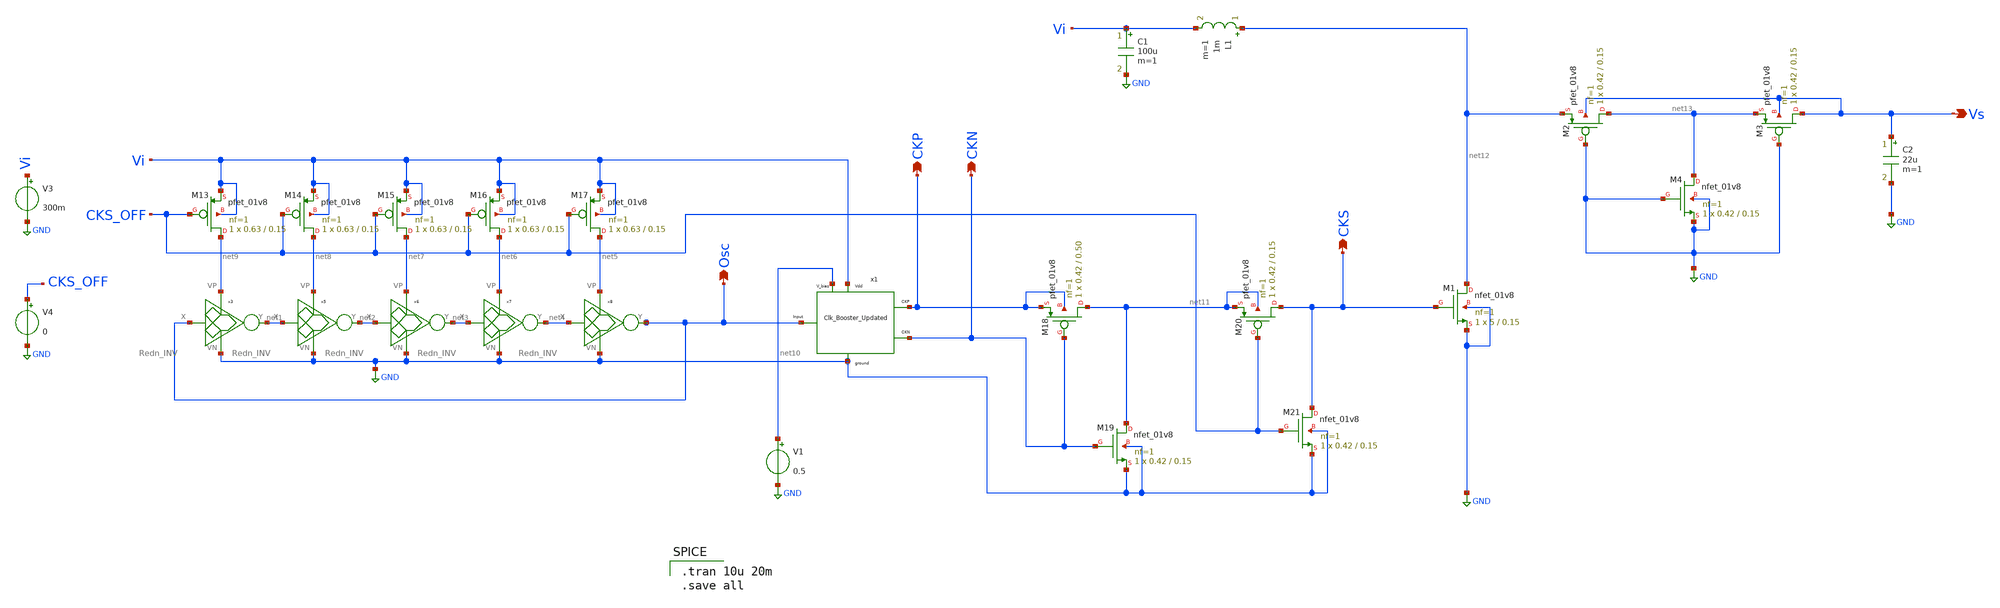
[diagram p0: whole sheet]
** sch_path: Blocks/StartupConverter/Startup_Converter1.sch
**.subckt Startup_Converter1 CKP CKN Osc CKS Vs
*.opin CKP
*.opin CKN
*.opin Osc
*.opin CKS
*.opin Vs
V3 Vi GND 300m
x3 Osc net1 net9 GND Redn_INV
x5 net1 net2 net8 GND Redn_INV
x6 net2 net3 net7 GND Redn_INV
x7 net3 net4 net6 GND Redn_INV
x8 net4 Osc net5 GND Redn_INV
XM13 net9 CKS_OFF Vi Vi sky130_fd_pr__pfet_01v8 L=0.15 W=0.63 nf=1 ad='int((nf+1)/2) * W/nf * 0.29' as='int((nf+2)/2) * W/nf * 0.29'
+ pd='2*int((nf+1)/2) * (W/nf + 0.29)' ps='2*int((nf+2)/2) * (W/nf + 0.29)' nrd='0.29 / W' nrs='0.29 / W'
+ sa=0 sb=0 sd=0 mult=1 m=1
XM14 net8 CKS_OFF Vi Vi sky130_fd_pr__pfet_01v8 L=0.15 W=0.63 nf=1 ad='int((nf+1)/2) * W/nf * 0.29' as='int((nf+2)/2) * W/nf * 0.29'
+ pd='2*int((nf+1)/2) * (W/nf + 0.29)' ps='2*int((nf+2)/2) * (W/nf + 0.29)' nrd='0.29 / W' nrs='0.29 / W'
+ sa=0 sb=0 sd=0 mult=1 m=1
XM15 net7 CKS_OFF Vi Vi sky130_fd_pr__pfet_01v8 L=0.15 W=0.63 nf=1 ad='int((nf+1)/2) * W/nf * 0.29' as='int((nf+2)/2) * W/nf * 0.29'
+ pd='2*int((nf+1)/2) * (W/nf + 0.29)' ps='2*int((nf+2)/2) * (W/nf + 0.29)' nrd='0.29 / W' nrs='0.29 / W'
+ sa=0 sb=0 sd=0 mult=1 m=1
XM16 net6 CKS_OFF Vi Vi sky130_fd_pr__pfet_01v8 L=0.15 W=0.63 nf=1 ad='int((nf+1)/2) * W/nf * 0.29' as='int((nf+2)/2) * W/nf * 0.29'
+ pd='2*int((nf+1)/2) * (W/nf + 0.29)' ps='2*int((nf+2)/2) * (W/nf + 0.29)' nrd='0.29 / W' nrs='0.29 / W'
+ sa=0 sb=0 sd=0 mult=1 m=1
XM17 net5 CKS_OFF Vi Vi sky130_fd_pr__pfet_01v8 L=0.15 W=0.63 nf=1 ad='int((nf+1)/2) * W/nf * 0.29' as='int((nf+2)/2) * W/nf * 0.29'
+ pd='2*int((nf+1)/2) * (W/nf + 0.29)' ps='2*int((nf+2)/2) * (W/nf + 0.29)' nrd='0.29 / W' nrs='0.29 / W'
+ sa=0 sb=0 sd=0 mult=1 m=1
V4 CKS_OFF GND 0
V1 net10 GND 0.5
XM18 net11 CKN CKP CKP sky130_fd_pr__pfet_01v8 L=0.50 W=0.42 nf=1 ad='int((nf+1)/2) * W/nf * 0.29' as='int((nf+2)/2) * W/nf * 0.29'
+ pd='2*int((nf+1)/2) * (W/nf + 0.29)' ps='2*int((nf+2)/2) * (W/nf + 0.29)' nrd='0.29 / W' nrs='0.29 / W'
+ sa=0 sb=0 sd=0 mult=1 m=1
XM19 net11 CKN GND GND sky130_fd_pr__nfet_01v8 L=0.15 W=0.42 nf=1 ad='int((nf+1)/2) * W/nf * 0.29' as='int((nf+2)/2) * W/nf * 0.29'
+ pd='2*int((nf+1)/2) * (W/nf + 0.29)' ps='2*int((nf+2)/2) * (W/nf + 0.29)' nrd='0.29 / W' nrs='0.29 / W'
+ sa=0 sb=0 sd=0 mult=1 m=1
XM21 CKS CKS_OFF GND GND sky130_fd_pr__nfet_01v8 L=0.15 W=0.42 nf=1 ad='int((nf+1)/2) * W/nf * 0.29'
+ as='int((nf+2)/2) * W/nf * 0.29' pd='2*int((nf+1)/2) * (W/nf + 0.29)' ps='2*int((nf+2)/2) * (W/nf + 0.29)'
+ nrd='0.29 / W' nrs='0.29 / W' sa=0 sb=0 sd=0 mult=1 m=1
XM20 CKS CKS_OFF net11 net11 sky130_fd_pr__pfet_01v8 L=0.15 W=0.42 nf=1 ad='int((nf+1)/2) * W/nf * 0.29'
+ as='int((nf+2)/2) * W/nf * 0.29' pd='2*int((nf+1)/2) * (W/nf + 0.29)' ps='2*int((nf+2)/2) * (W/nf + 0.29)'
+ nrd='0.29 / W' nrs='0.29 / W' sa=0 sb=0 sd=0 mult=1 m=1
x1 Osc Vi GND CKP CKN net10 Clk_Booster_Updated
C1 Vi GND 100u m=1
L1 net12 Vi 1m m=1
XM1 net12 CKS GND GND sky130_fd_pr__nfet_01v8 L=0.15 W=5 nf=1 ad='int((nf+1)/2) * W/nf * 0.29' as='int((nf+2)/2) * W/nf * 0.29'
+ pd='2*int((nf+1)/2) * (W/nf + 0.29)' ps='2*int((nf+2)/2) * (W/nf + 0.29)' nrd='0.29 / W' nrs='0.29 / W'
+ sa=0 sb=0 sd=0 mult=1 m=1
XM2 net13 GND net12 Vs sky130_fd_pr__pfet_01v8 L=0.15 W=0.42 nf=1 ad='int((nf+1)/2) * W/nf * 0.29' as='int((nf+2)/2) * W/nf * 0.29'
+ pd='2*int((nf+1)/2) * (W/nf + 0.29)' ps='2*int((nf+2)/2) * (W/nf + 0.29)' nrd='0.29 / W' nrs='0.29 / W'
+ sa=0 sb=0 sd=0 mult=1 m=1
XM3 Vs GND net13 Vs sky130_fd_pr__pfet_01v8 L=0.15 W=0.42 nf=1 ad='int((nf+1)/2) * W/nf * 0.29' as='int((nf+2)/2) * W/nf * 0.29'
+ pd='2*int((nf+1)/2) * (W/nf + 0.29)' ps='2*int((nf+2)/2) * (W/nf + 0.29)' nrd='0.29 / W' nrs='0.29 / W'
+ sa=0 sb=0 sd=0 mult=1 m=1
XM4 net13 GND GND GND sky130_fd_pr__nfet_01v8 L=0.15 W=0.42 nf=1 ad='int((nf+1)/2) * W/nf * 0.29' as='int((nf+2)/2) * W/nf * 0.29'
+ pd='2*int((nf+1)/2) * (W/nf + 0.29)' ps='2*int((nf+2)/2) * (W/nf + 0.29)' nrd='0.29 / W' nrs='0.29 / W'
+ sa=0 sb=0 sd=0 mult=1 m=1
C2 Vs GND 22u m=1
**** begin user architecture code

** opencircuitdesign pdks install
.lib $::SKYWATER_MODELS/sky130.lib.spice tt



.tran 10u 20m
.save all

**** end user architecture code
**.ends

* expanding   symbol:  Pico_project/Rdn_INV/Redn_INV.sym # of pins=4
** sym_path: component/Reduntant_Inverter/Redn_INV.sym
** sch_path: component/Reduntant_Inverter/Redn_INV.sch
.subckt Redn_INV X Y VP VN
*.opin Y
*.ipin X
*.iopin VP
*.iopin VN
XM15 net4 X VN VN sky130_fd_pr__nfet_01v8_lvt L=0.15 W=1 nf=1 ad='int((nf+1)/2) * W/nf * 0.29' as='int((nf+2)/2) * W/nf * 0.29'
+ pd='2*int((nf+1)/2) * (W/nf + 0.29)' ps='2*int((nf+2)/2) * (W/nf + 0.29)' nrd='0.29 / W' nrs='0.29 / W'
+ sa=0 sb=0 sd=0 mult=1 m=1
XM1 net5 X net3 VN sky130_fd_pr__nfet_01v8_lvt L=0.15 W=3.25 nf=1 ad='int((nf+1)/2) * W/nf * 0.29' as='int((nf+2)/2) * W/nf * 0.29'
+ pd='2*int((nf+1)/2) * (W/nf + 0.29)' ps='2*int((nf+2)/2) * (W/nf + 0.29)' nrd='0.29 / W' nrs='0.29 / W'
+ sa=0 sb=0 sd=0 mult=1 m=1
XM16 Y X net6 VN sky130_fd_pr__nfet_01v8_lvt L=0.15 W=6.5 nf=1 ad='int((nf+1)/2) * W/nf * 0.29' as='int((nf+2)/2) * W/nf * 0.29'
+ pd='2*int((nf+1)/2) * (W/nf + 0.29)' ps='2*int((nf+2)/2) * (W/nf + 0.29)' nrd='0.29 / W' nrs='0.29 / W'
+ sa=0 sb=0 sd=0 mult=1 m=1
XM17 net3 X VN VN sky130_fd_pr__nfet_01v8_lvt L=0.15 W=3.25 nf=1 ad='int((nf+1)/2) * W/nf * 0.29' as='int((nf+2)/2) * W/nf * 0.29'
+ pd='2*int((nf+1)/2) * (W/nf + 0.29)' ps='2*int((nf+2)/2) * (W/nf + 0.29)' nrd='0.29 / W' nrs='0.29 / W'
+ sa=0 sb=0 sd=0 mult=1 m=1
XM18 net2 X VN VN sky130_fd_pr__nfet_01v8_lvt L=0.15 W=1.5 nf=1 ad='int((nf+1)/2) * W/nf * 0.29' as='int((nf+2)/2) * W/nf * 0.29'
+ pd='2*int((nf+1)/2) * (W/nf + 0.29)' ps='2*int((nf+2)/2) * (W/nf + 0.29)' nrd='0.29 / W' nrs='0.29 / W'
+ sa=0 sb=0 sd=0 mult=1 m=1
XM19 net1 X VN VN sky130_fd_pr__nfet_01v8_lvt L=0.15 W=6.5 nf=1 ad='int((nf+1)/2) * W/nf * 0.29' as='int((nf+2)/2) * W/nf * 0.29'
+ pd='2*int((nf+1)/2) * (W/nf + 0.29)' ps='2*int((nf+2)/2) * (W/nf + 0.29)' nrd='0.29 / W' nrs='0.29 / W'
+ sa=0 sb=0 sd=0 mult=1 m=1
XM20 net6 X net1 VN sky130_fd_pr__nfet_01v8_lvt L=0.15 W=6.5 nf=1 ad='int((nf+1)/2) * W/nf * 0.29' as='int((nf+2)/2) * W/nf * 0.29'
+ pd='2*int((nf+1)/2) * (W/nf + 0.29)' ps='2*int((nf+2)/2) * (W/nf + 0.29)' nrd='0.29 / W' nrs='0.29 / W'
+ sa=0 sb=0 sd=0 mult=1 m=1
XM2 net4 X VP VP sky130_fd_pr__pfet_01v8 L=0.15 W=10 nf=1 ad='int((nf+1)/2) * W/nf * 0.29' as='int((nf+2)/2) * W/nf * 0.29'
+ pd='2*int((nf+1)/2) * (W/nf + 0.29)' ps='2*int((nf+2)/2) * (W/nf + 0.29)' nrd='0.29 / W' nrs='0.29 / W'
+ sa=0 sb=0 sd=0 mult=1 m=1
XM5 net5 X net4 net4 sky130_fd_pr__pfet_01v8 L=0.15 W=10 nf=1 ad='int((nf+1)/2) * W/nf * 0.29' as='int((nf+2)/2) * W/nf * 0.29'
+ pd='2*int((nf+1)/2) * (W/nf + 0.29)' ps='2*int((nf+2)/2) * (W/nf + 0.29)' nrd='0.29 / W' nrs='0.29 / W'
+ sa=0 sb=0 sd=0 mult=1 m=1
XM6 Y X net5 VP sky130_fd_pr__pfet_01v8 L=0.15 W=10 nf=1 ad='int((nf+1)/2) * W/nf * 0.29' as='int((nf+2)/2) * W/nf * 0.29'
+ pd='2*int((nf+1)/2) * (W/nf + 0.29)' ps='2*int((nf+2)/2) * (W/nf + 0.29)' nrd='0.29 / W' nrs='0.29 / W'
+ sa=0 sb=0 sd=0 mult=1 m=1
XM8 net3 X VP VP sky130_fd_pr__pfet_01v8 L=0.15 W=2 nf=1 ad='int((nf+1)/2) * W/nf * 0.29' as='int((nf+2)/2) * W/nf * 0.29'
+ pd='2*int((nf+1)/2) * (W/nf + 0.29)' ps='2*int((nf+2)/2) * (W/nf + 0.29)' nrd='0.29 / W' nrs='0.29 / W'
+ sa=0 sb=0 sd=0 mult=1 m=1
XM12 net2 X VP VP sky130_fd_pr__pfet_01v8 L=0.15 W=5 nf=1 ad='int((nf+1)/2) * W/nf * 0.29' as='int((nf+2)/2) * W/nf * 0.29'
+ pd='2*int((nf+1)/2) * (W/nf + 0.29)' ps='2*int((nf+2)/2) * (W/nf + 0.29)' nrd='0.29 / W' nrs='0.29 / W'
+ sa=0 sb=0 sd=0 mult=1 m=1
XM14 net6 X net2 VP sky130_fd_pr__pfet_01v8 L=0.15 W=5 nf=1 ad='int((nf+1)/2) * W/nf * 0.29' as='int((nf+2)/2) * W/nf * 0.29'
+ pd='2*int((nf+1)/2) * (W/nf + 0.29)' ps='2*int((nf+2)/2) * (W/nf + 0.29)' nrd='0.29 / W' nrs='0.29 / W'
+ sa=0 sb=0 sd=0 mult=1 m=1
XM21 net1 X VP VP sky130_fd_pr__pfet_01v8 L=0.15 W=1.5 nf=1 ad='int((nf+1)/2) * W/nf * 0.29' as='int((nf+2)/2) * W/nf * 0.29'
+ pd='2*int((nf+1)/2) * (W/nf + 0.29)' ps='2*int((nf+2)/2) * (W/nf + 0.29)' nrd='0.29 / W' nrs='0.29 / W'
+ sa=0 sb=0 sd=0 mult=1 m=1
.ends


* expanding   symbol:  Pico_project/Clock_Booster_new/Clk_Booster_Updated.sym # of pins=6
** sym_path: Blocks/Clock_Booster_new/Clk_Booster_Updated.sym
** sch_path: Blocks/Clock_Booster_new/Clk_Booster_Updated.sch
.subckt Clk_Booster_Updated X VP VN CKP CKN V_bias
*.opin CKP
*.opin CKN
*.iopin VP
*.iopin V_bias
*.ipin X
*.iopin VN
C1 net23 net13 100f m=1
XM1 net15 net6 net11 V_bias sky130_fd_pr__pfet_01v8 L=0.15 W=0.42 nf=1 ad='int((nf+1)/2) * W/nf * 0.29'
+ as='int((nf+2)/2) * W/nf * 0.29' pd='2*int((nf+1)/2) * (W/nf + 0.29)' ps='2*int((nf+2)/2) * (W/nf + 0.29)'
+ nrd='0.29 / W' nrs='0.29 / W' sa=0 sb=0 sd=0 mult=1 m=1
XM3 net6 net5 net24 V_bias sky130_fd_pr__pfet_01v8 L=0.15 W=0.42 nf=1 ad='int((nf+1)/2) * W/nf * 0.29'
+ as='int((nf+2)/2) * W/nf * 0.29' pd='2*int((nf+1)/2) * (W/nf + 0.29)' ps='2*int((nf+2)/2) * (W/nf + 0.29)'
+ nrd='0.29 / W' nrs='0.29 / W' sa=0 sb=0 sd=0 mult=1 m=1
XM4 net6 net5 VN VN sky130_fd_pr__nfet_01v8 L=0.15 W=2 nf=1 ad='int((nf+1)/2) * W/nf * 0.29' as='int((nf+2)/2) * W/nf * 0.29'
+ pd='2*int((nf+1)/2) * (W/nf + 0.29)' ps='2*int((nf+2)/2) * (W/nf + 0.29)' nrd='0.29 / W' nrs='0.29 / W'
+ sa=0 sb=0 sd=0 mult=1 m=1
XM2 net16 CKP net14 V_bias sky130_fd_pr__pfet_01v8 L=0.15 W=0.42 nf=1 ad='int((nf+1)/2) * W/nf * 0.29'
+ as='int((nf+2)/2) * W/nf * 0.29' pd='2*int((nf+1)/2) * (W/nf + 0.29)' ps='2*int((nf+2)/2) * (W/nf + 0.29)'
+ nrd='0.29 / W' nrs='0.29 / W' sa=0 sb=0 sd=0 mult=1 m=1
XM5 CKP net5 net25 V_bias sky130_fd_pr__pfet_01v8 L=0.15 W=0.42 nf=1 ad='int((nf+1)/2) * W/nf * 0.29'
+ as='int((nf+2)/2) * W/nf * 0.29' pd='2*int((nf+1)/2) * (W/nf + 0.29)' ps='2*int((nf+2)/2) * (W/nf + 0.29)'
+ nrd='0.29 / W' nrs='0.29 / W' sa=0 sb=0 sd=0 mult=1 m=1
XM6 CKP net5 VN VN sky130_fd_pr__nfet_01v8 L=0.15 W=1.26 nf=1 ad='int((nf+1)/2) * W/nf * 0.29' as='int((nf+2)/2) * W/nf * 0.29'
+ pd='2*int((nf+1)/2) * (W/nf + 0.29)' ps='2*int((nf+2)/2) * (W/nf + 0.29)' nrd='0.29 / W' nrs='0.29 / W'
+ sa=0 sb=0 sd=0 mult=1 m=1
C3 net10 net7 100f m=1
XM8 net22 net4 net7 V_bias sky130_fd_pr__pfet_01v8 L=0.15 W=0.42 nf=1 ad='int((nf+1)/2) * W/nf * 0.29'
+ as='int((nf+2)/2) * W/nf * 0.29' pd='2*int((nf+1)/2) * (W/nf + 0.29)' ps='2*int((nf+2)/2) * (W/nf + 0.29)'
+ nrd='0.29 / W' nrs='0.29 / W' sa=0 sb=0 sd=0 mult=1 m=1
XM9 net9 net4 VN VN sky130_fd_pr__nfet_01v8 L=0.15 W=2 nf=1 ad='int((nf+1)/2) * W/nf * 0.29' as='int((nf+2)/2) * W/nf * 0.29'
+ pd='2*int((nf+1)/2) * (W/nf + 0.29)' ps='2*int((nf+2)/2) * (W/nf + 0.29)' nrd='0.29 / W' nrs='0.29 / W'
+ sa=0 sb=0 sd=0 mult=1 m=1
XM10 net8 CKN net18 V_bias sky130_fd_pr__pfet_01v8 L=0.15 W=0.42 nf=1 ad='int((nf+1)/2) * W/nf * 0.29'
+ as='int((nf+2)/2) * W/nf * 0.29' pd='2*int((nf+1)/2) * (W/nf + 0.29)' ps='2*int((nf+2)/2) * (W/nf + 0.29)'
+ nrd='0.29 / W' nrs='0.29 / W' sa=0 sb=0 sd=0 mult=1 m=1
XM11 net21 net4 net8 V_bias sky130_fd_pr__pfet_01v8 L=0.15 W=0.42 nf=1 ad='int((nf+1)/2) * W/nf * 0.29'
+ as='int((nf+2)/2) * W/nf * 0.29' pd='2*int((nf+1)/2) * (W/nf + 0.29)' ps='2*int((nf+2)/2) * (W/nf + 0.29)'
+ nrd='0.29 / W' nrs='0.29 / W' sa=0 sb=0 sd=0 mult=1 m=1
XM12 CKN net4 VN VN sky130_fd_pr__nfet_01v8 L=0.15 W=1.26 nf=1 ad='int((nf+1)/2) * W/nf * 0.29' as='int((nf+2)/2) * W/nf * 0.29'
+ pd='2*int((nf+1)/2) * (W/nf + 0.29)' ps='2*int((nf+2)/2) * (W/nf + 0.29)' nrd='0.29 / W' nrs='0.29 / W'
+ sa=0 sb=0 sd=0 mult=1 m=1
C4 net9 net8 100f m=1
XM7 net7 net9 net19 V_bias sky130_fd_pr__pfet_01v8 L=0.15 W=0.42 nf=1 ad='int((nf+1)/2) * W/nf * 0.29'
+ as='int((nf+2)/2) * W/nf * 0.29' pd='2*int((nf+1)/2) * (W/nf + 0.29)' ps='2*int((nf+2)/2) * (W/nf + 0.29)'
+ nrd='0.29 / W' nrs='0.29 / W' sa=0 sb=0 sd=0 mult=1 m=1
x4 net5 net23 VP VN Redn_INV
x1 X net1 VP VN Redn_INV
x2 net1 net2 VP VN Redn_INV
x15 net2 net5 VP VN Redn_INV
x22 net3 net4 VP VN Redn_INV
x23 net4 net10 VP VN Redn_INV
XM18 net13 net6 net15 V_bias sky130_fd_pr__pfet_01v8 L=0.15 W=0.42 nf=1 ad='int((nf+1)/2) * W/nf * 0.29'
+ as='int((nf+2)/2) * W/nf * 0.29' pd='2*int((nf+1)/2) * (W/nf + 0.29)' ps='2*int((nf+2)/2) * (W/nf + 0.29)'
+ nrd='0.29 / W' nrs='0.29 / W' sa=0 sb=0 sd=0 mult=1 m=1
XM21 net12 CKP net16 V_bias sky130_fd_pr__pfet_01v8 L=0.15 W=0.42 nf=1 ad='int((nf+1)/2) * W/nf * 0.29'
+ as='int((nf+2)/2) * W/nf * 0.29' pd='2*int((nf+1)/2) * (W/nf + 0.29)' ps='2*int((nf+2)/2) * (W/nf + 0.29)'
+ nrd='0.29 / W' nrs='0.29 / W' sa=0 sb=0 sd=0 mult=1 m=1
C2 net6 net12 100f m=1
XM19 net11 net6 VP V_bias sky130_fd_pr__pfet_01v8 L=0.15 W=0.42 nf=1 ad='int((nf+1)/2) * W/nf * 0.29'
+ as='int((nf+2)/2) * W/nf * 0.29' pd='2*int((nf+1)/2) * (W/nf + 0.29)' ps='2*int((nf+2)/2) * (W/nf + 0.29)'
+ nrd='0.29 / W' nrs='0.29 / W' sa=0 sb=0 sd=0 mult=1 m=1
XM20 net14 CKP VP V_bias sky130_fd_pr__pfet_01v8 L=0.15 W=0.42 nf=1 ad='int((nf+1)/2) * W/nf * 0.29'
+ as='int((nf+2)/2) * W/nf * 0.29' pd='2*int((nf+1)/2) * (W/nf + 0.29)' ps='2*int((nf+2)/2) * (W/nf + 0.29)'
+ nrd='0.29 / W' nrs='0.29 / W' sa=0 sb=0 sd=0 mult=1 m=1
XM22 net25 net5 net12 V_bias sky130_fd_pr__pfet_01v8 L=0.15 W=0.42 nf=1 ad='int((nf+1)/2) * W/nf * 0.29'
+ as='int((nf+2)/2) * W/nf * 0.29' pd='2*int((nf+1)/2) * (W/nf + 0.29)' ps='2*int((nf+2)/2) * (W/nf + 0.29)'
+ nrd='0.29 / W' nrs='0.29 / W' sa=0 sb=0 sd=0 mult=1 m=1
XM23 net24 net5 net13 V_bias sky130_fd_pr__pfet_01v8 L=0.15 W=0.42 nf=1 ad='int((nf+1)/2) * W/nf * 0.29'
+ as='int((nf+2)/2) * W/nf * 0.29' pd='2*int((nf+1)/2) * (W/nf + 0.29)' ps='2*int((nf+2)/2) * (W/nf + 0.29)'
+ nrd='0.29 / W' nrs='0.29 / W' sa=0 sb=0 sd=0 mult=1 m=1
XM24 net19 net9 net20 V_bias sky130_fd_pr__pfet_01v8 L=0.15 W=0.42 nf=1 ad='int((nf+1)/2) * W/nf * 0.29'
+ as='int((nf+2)/2) * W/nf * 0.29' pd='2*int((nf+1)/2) * (W/nf + 0.29)' ps='2*int((nf+2)/2) * (W/nf + 0.29)'
+ nrd='0.29 / W' nrs='0.29 / W' sa=0 sb=0 sd=0 mult=1 m=1
XM25 net20 net9 VP V_bias sky130_fd_pr__pfet_01v8 L=0.15 W=0.42 nf=1 ad='int((nf+1)/2) * W/nf * 0.29'
+ as='int((nf+2)/2) * W/nf * 0.29' pd='2*int((nf+1)/2) * (W/nf + 0.29)' ps='2*int((nf+2)/2) * (W/nf + 0.29)'
+ nrd='0.29 / W' nrs='0.29 / W' sa=0 sb=0 sd=0 mult=1 m=1
XM26 net18 CKN net17 V_bias sky130_fd_pr__pfet_01v8 L=0.15 W=0.42 nf=1 ad='int((nf+1)/2) * W/nf * 0.29'
+ as='int((nf+2)/2) * W/nf * 0.29' pd='2*int((nf+1)/2) * (W/nf + 0.29)' ps='2*int((nf+2)/2) * (W/nf + 0.29)'
+ nrd='0.29 / W' nrs='0.29 / W' sa=0 sb=0 sd=0 mult=1 m=1
XM27 net17 CKN VP V_bias sky130_fd_pr__pfet_01v8 L=0.15 W=0.42 nf=1 ad='int((nf+1)/2) * W/nf * 0.29'
+ as='int((nf+2)/2) * W/nf * 0.29' pd='2*int((nf+1)/2) * (W/nf + 0.29)' ps='2*int((nf+2)/2) * (W/nf + 0.29)'
+ nrd='0.29 / W' nrs='0.29 / W' sa=0 sb=0 sd=0 mult=1 m=1
XM28 net9 net4 net22 V_bias sky130_fd_pr__pfet_01v8 L=0.15 W=0.42 nf=1 ad='int((nf+1)/2) * W/nf * 0.29'
+ as='int((nf+2)/2) * W/nf * 0.29' pd='2*int((nf+1)/2) * (W/nf + 0.29)' ps='2*int((nf+2)/2) * (W/nf + 0.29)'
+ nrd='0.29 / W' nrs='0.29 / W' sa=0 sb=0 sd=0 mult=1 m=1
XM29 CKN net4 net21 V_bias sky130_fd_pr__pfet_01v8 L=0.15 W=0.42 nf=1 ad='int((nf+1)/2) * W/nf * 0.29'
+ as='int((nf+2)/2) * W/nf * 0.29' pd='2*int((nf+1)/2) * (W/nf + 0.29)' ps='2*int((nf+2)/2) * (W/nf + 0.29)'
+ nrd='0.29 / W' nrs='0.29 / W' sa=0 sb=0 sd=0 mult=1 m=1
x9 net2 net3 VP VN Redn_INV
.ends

.GLOBAL GND
.end
